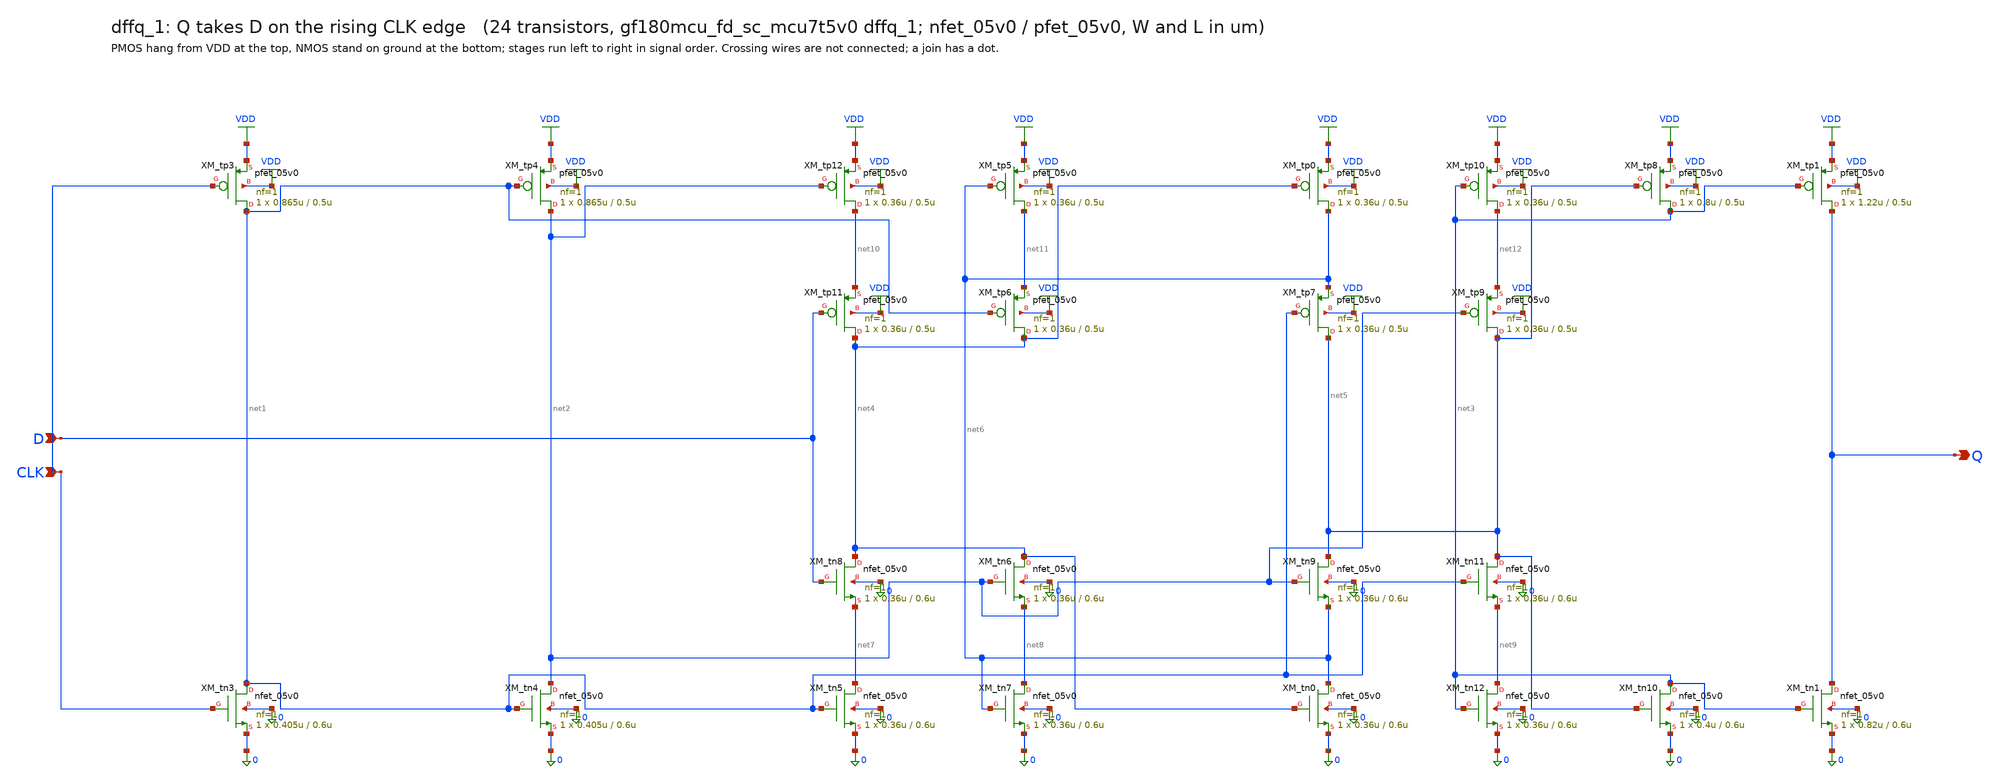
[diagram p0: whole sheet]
** sch_path: xschem/cells_tx/dffq_1.sch
**.subckt dffq_1 D CLK Q
*.ipin D
*.ipin CLK
*.opin Q
XM_tn3 net1 CLK 0 0 nfet_05v0 L=0.6u W=0.405u nf=1 ad=2.025e-13 as=2.025e-13 pd=1.81e-06 ps=1.81e-06
+ nrd=0 nrs=0 sa=0 sb=0 sd=0 m=1
XM_tn4 net2 net1 0 0 nfet_05v0 L=0.6u W=0.405u nf=1 ad=2.025e-13 as=2.025e-13 pd=1.81e-06
+ ps=1.81e-06 nrd=0 nrs=0 sa=0 sb=0 sd=0 m=1
XM_tn5 net7 net1 0 0 nfet_05v0 L=0.6u W=0.36u nf=1 ad=1.8e-13 as=1.8e-13 pd=1.72e-06 ps=1.72e-06
+ nrd=0 nrs=0 sa=0 sb=0 sd=0 m=1
XM_tn8 net4 D net7 0 nfet_05v0 L=0.6u W=0.36u nf=1 ad=1.8e-13 as=1.8e-13 pd=1.72e-06 ps=1.72e-06
+ nrd=0 nrs=0 sa=0 sb=0 sd=0 m=1
XM_tn6 net4 net2 net8 0 nfet_05v0 L=0.6u W=0.36u nf=1 ad=1.8e-13 as=1.8e-13 pd=1.72e-06 ps=1.72e-06
+ nrd=0 nrs=0 sa=0 sb=0 sd=0 m=1
XM_tn7 net8 net6 0 0 nfet_05v0 L=0.6u W=0.36u nf=1 ad=1.8e-13 as=1.8e-13 pd=1.72e-06 ps=1.72e-06
+ nrd=0 nrs=0 sa=0 sb=0 sd=0 m=1
XM_tn0 net6 net4 0 0 nfet_05v0 L=0.6u W=0.36u nf=1 ad=1.8e-13 as=1.8e-13 pd=1.72e-06 ps=1.72e-06
+ nrd=0 nrs=0 sa=0 sb=0 sd=0 m=1
XM_tn9 net5 net2 net6 0 nfet_05v0 L=0.6u W=0.36u nf=1 ad=1.8e-13 as=1.8e-13 pd=1.72e-06 ps=1.72e-06
+ nrd=0 nrs=0 sa=0 sb=0 sd=0 m=1
XM_tn11 net5 net1 net9 0 nfet_05v0 L=0.6u W=0.36u nf=1 ad=1.8e-13 as=1.8e-13 pd=1.72e-06 ps=1.72e-06
+ nrd=0 nrs=0 sa=0 sb=0 sd=0 m=1
XM_tn12 net9 net3 0 0 nfet_05v0 L=0.6u W=0.36u nf=1 ad=1.8e-13 as=1.8e-13 pd=1.72e-06 ps=1.72e-06
+ nrd=0 nrs=0 sa=0 sb=0 sd=0 m=1
XM_tn10 net3 net5 0 0 nfet_05v0 L=0.6u W=0.4u nf=1 ad=2e-13 as=2e-13 pd=1.8e-06 ps=1.8e-06 nrd=0
+ nrs=0 sa=0 sb=0 sd=0 m=1
XM_tn1 Q net3 0 0 nfet_05v0 L=0.6u W=0.82u nf=1 ad=4.1e-13 as=4.1e-13 pd=2.64e-06 ps=2.64e-06 nrd=0
+ nrs=0 sa=0 sb=0 sd=0 m=1
XM_tp3 net1 CLK VDD VDD pfet_05v0 L=0.5u W=0.865u nf=1 ad=4.325e-13 as=4.325e-13 pd=2.73e-06
+ ps=2.73e-06 nrd=0 nrs=0 sa=0 sb=0 sd=0 m=1
XM_tp4 net2 net1 VDD VDD pfet_05v0 L=0.5u W=0.865u nf=1 ad=4.325e-13 as=4.325e-13 pd=2.73e-06
+ ps=2.73e-06 nrd=0 nrs=0 sa=0 sb=0 sd=0 m=1
XM_tp12 net10 net2 VDD VDD pfet_05v0 L=0.5u W=0.36u nf=1 ad=1.8e-13 as=1.8e-13 pd=1.72e-06
+ ps=1.72e-06 nrd=0 nrs=0 sa=0 sb=0 sd=0 m=1
XM_tp11 net4 D net10 VDD pfet_05v0 L=0.5u W=0.36u nf=1 ad=1.8e-13 as=1.8e-13 pd=1.72e-06 ps=1.72e-06
+ nrd=0 nrs=0 sa=0 sb=0 sd=0 m=1
XM_tp6 net4 net1 net11 VDD pfet_05v0 L=0.5u W=0.36u nf=1 ad=1.8e-13 as=1.8e-13 pd=1.72e-06
+ ps=1.72e-06 nrd=0 nrs=0 sa=0 sb=0 sd=0 m=1
XM_tp5 net11 net6 VDD VDD pfet_05v0 L=0.5u W=0.36u nf=1 ad=1.8e-13 as=1.8e-13 pd=1.72e-06
+ ps=1.72e-06 nrd=0 nrs=0 sa=0 sb=0 sd=0 m=1
XM_tp0 net6 net4 VDD VDD pfet_05v0 L=0.5u W=0.36u nf=1 ad=1.8e-13 as=1.8e-13 pd=1.72e-06 ps=1.72e-06
+ nrd=0 nrs=0 sa=0 sb=0 sd=0 m=1
XM_tp7 net5 net1 net6 VDD pfet_05v0 L=0.5u W=0.36u nf=1 ad=1.8e-13 as=1.8e-13 pd=1.72e-06
+ ps=1.72e-06 nrd=0 nrs=0 sa=0 sb=0 sd=0 m=1
XM_tp9 net5 net2 net12 VDD pfet_05v0 L=0.5u W=0.36u nf=1 ad=1.8e-13 as=1.8e-13 pd=1.72e-06
+ ps=1.72e-06 nrd=0 nrs=0 sa=0 sb=0 sd=0 m=1
XM_tp10 net12 net3 VDD VDD pfet_05v0 L=0.5u W=0.36u nf=1 ad=1.8e-13 as=1.8e-13 pd=1.72e-06
+ ps=1.72e-06 nrd=0 nrs=0 sa=0 sb=0 sd=0 m=1
XM_tp8 net3 net5 VDD VDD pfet_05v0 L=0.5u W=0.8u nf=1 ad=4e-13 as=4e-13 pd=2.6e-06 ps=2.6e-06 nrd=0
+ nrs=0 sa=0 sb=0 sd=0 m=1
XM_tp1 Q net3 VDD VDD pfet_05v0 L=0.5u W=1.22u nf=1 ad=6.1e-13 as=6.1e-13 pd=3.44e-06 ps=3.44e-06
+ nrd=0 nrs=0 sa=0 sb=0 sd=0 m=1
**.ends
.GLOBAL VDD
.end
